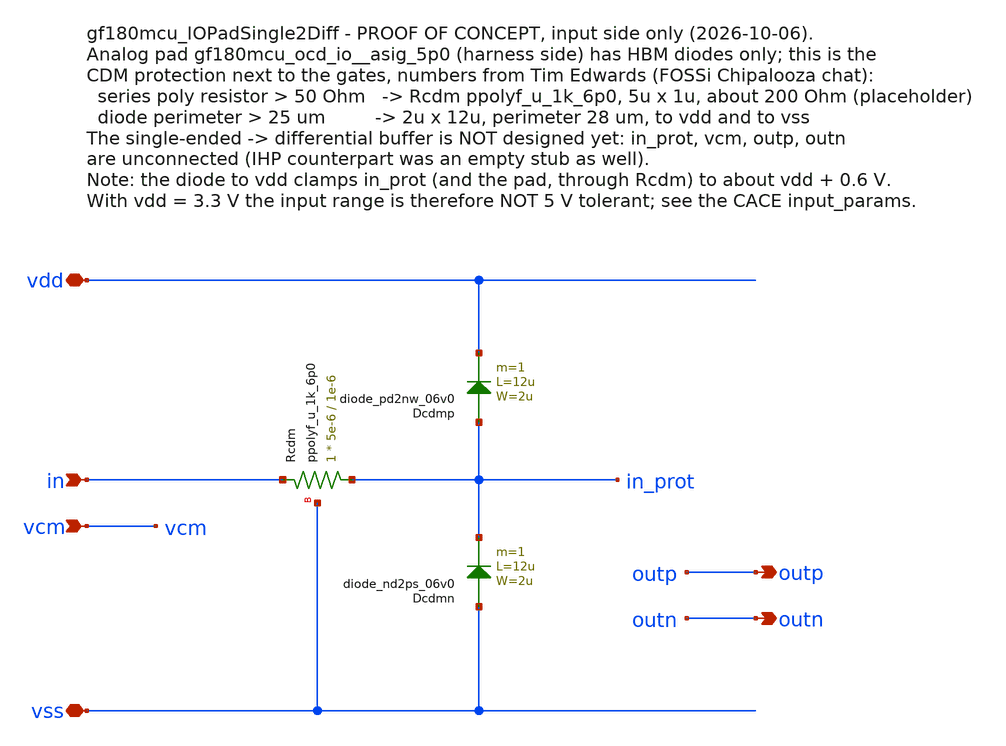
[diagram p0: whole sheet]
** sch_path: macros/gf180mcu_IOPadSingle2Diff/schematic/xschem/gf180mcu_IOPadSingle2Diff.sch
**.subckt gf180mcu_IOPadSingle2Diff vdd outp vcm in outn vss
*.iopin vdd
*.opin outp
*.ipin vcm
*.ipin in
*.opin outn
*.iopin vss
XRcdm in_prot in vss ppolyf_u_1k_6p0 r_width=5e-6 r_length=1e-6 m=1
Dcdmp in_prot vdd diode_pd2nw_06v0 area='2u * 12u ' pj='2*2u + 2*12u ' m=1
Dcdmn vss in_prot diode_nd2ps_06v0 area='2u * 12u ' pj='2*2u + 2*12u ' m=1
**.ends
.end
